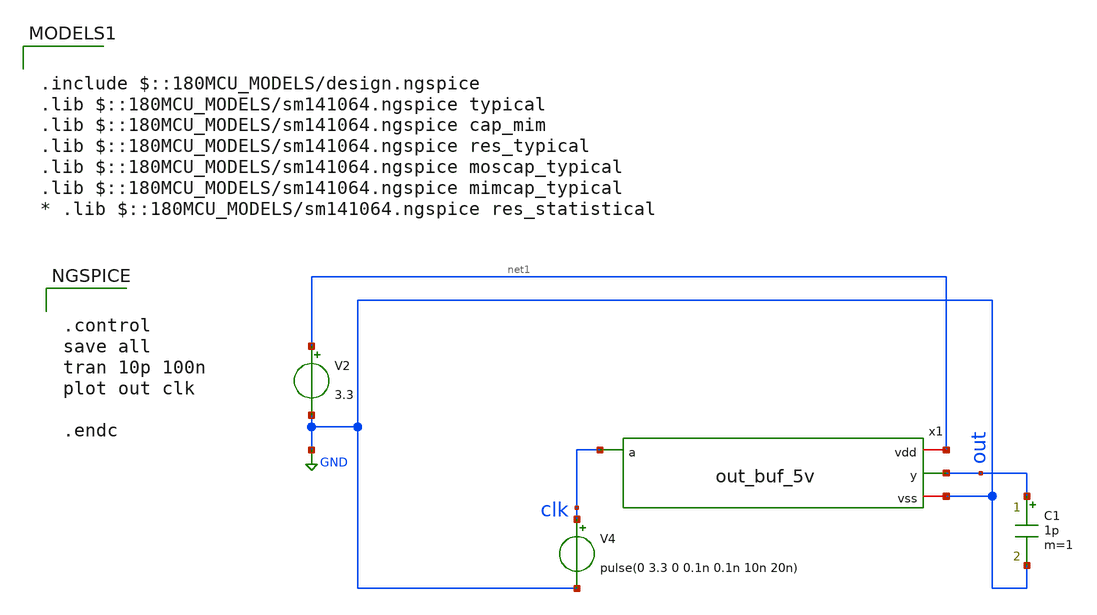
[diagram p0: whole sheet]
** sch_path: member_project/ice458/dynamic_comparator/xschem/out_buf_5v_tb.sch
**.subckt out_buf_5v_tb
V2 net1 GND 3.3
V4 clk GND pulse(0 3.3 0 0.1n 0.1n 10n 20n)
x1 net1 clk out GND out_buf_5v
C1 out GND 1p m=1
**** begin user architecture code


.control
save all
tran 10p 100n
plot out clk

.endc



.include $::180MCU_MODELS/design.ngspice
.lib $::180MCU_MODELS/sm141064.ngspice typical
.lib $::180MCU_MODELS/sm141064.ngspice cap_mim
.lib $::180MCU_MODELS/sm141064.ngspice res_typical
.lib $::180MCU_MODELS/sm141064.ngspice moscap_typical
.lib $::180MCU_MODELS/sm141064.ngspice mimcap_typical
* .lib $::180MCU_MODELS/sm141064.ngspice res_statistical

**** end user architecture code
**.ends

* expanding   symbol:  out_buf_5v.sym # of pins=4
** sym_path: member_project/ice458/dynamic_comparator/xschem/out_buf_5v.sym
** sch_path: member_project/ice458/dynamic_comparator/xschem/out_buf_5v.sch
.subckt out_buf_5v vdd a y vss
*.iopin vdd
*.iopin vss
*.ipin a
*.opin y
x1 vdd a net1 vss inv_5v
XM3 y net1 vss vss nfet_06v0 L=0.70u W=3u nf=1 ad='int((nf+1)/2) * W/nf * 0.18u' as='int((nf+2)/2) * W/nf * 0.18u'
+ pd='2*int((nf+1)/2) * (W/nf + 0.18u)' ps='2*int((nf+2)/2) * (W/nf + 0.18u)' nrd='0.18u / W' nrs='0.18u / W'
+ sa=0 sb=0 sd=0 m=1
XM5 y net1 vdd vdd pfet_05v0 L=0.7u W=9u nf=1 ad='int((nf+1)/2) * W/nf * 0.18u' as='int((nf+2)/2) * W/nf * 0.18u'
+ pd='2*int((nf+1)/2) * (W/nf + 0.18u)' ps='2*int((nf+2)/2) * (W/nf + 0.18u)' nrd='0.18u / W' nrs='0.18u / W'
+ sa=0 sb=0 sd=0 m=1
.ends


* expanding   symbol:  inv_5v.sym # of pins=4
** sym_path: member_project/ice458/dynamic_comparator/xschem/inv_5v.sym
** sch_path: member_project/ice458/dynamic_comparator/xschem/inv_5v.sch
.subckt inv_5v vdd a y vss
*.iopin vdd
*.iopin vss
*.ipin a
*.opin y
XM3 y a vss vss nfet_06v0 L=0.70u W=1u nf=1 ad='int((nf+1)/2) * W/nf * 0.18u' as='int((nf+2)/2) * W/nf * 0.18u'
+ pd='2*int((nf+1)/2) * (W/nf + 0.18u)' ps='2*int((nf+2)/2) * (W/nf + 0.18u)' nrd='0.18u / W' nrs='0.18u / W'
+ sa=0 sb=0 sd=0 m=1
XM5 y a vdd vdd pfet_05v0 L=0.7u W=3u nf=1 ad='int((nf+1)/2) * W/nf * 0.18u' as='int((nf+2)/2) * W/nf * 0.18u'
+ pd='2*int((nf+1)/2) * (W/nf + 0.18u)' ps='2*int((nf+2)/2) * (W/nf + 0.18u)' nrd='0.18u / W' nrs='0.18u / W'
+ sa=0 sb=0 sd=0 m=1
.ends

.GLOBAL GND
.end
